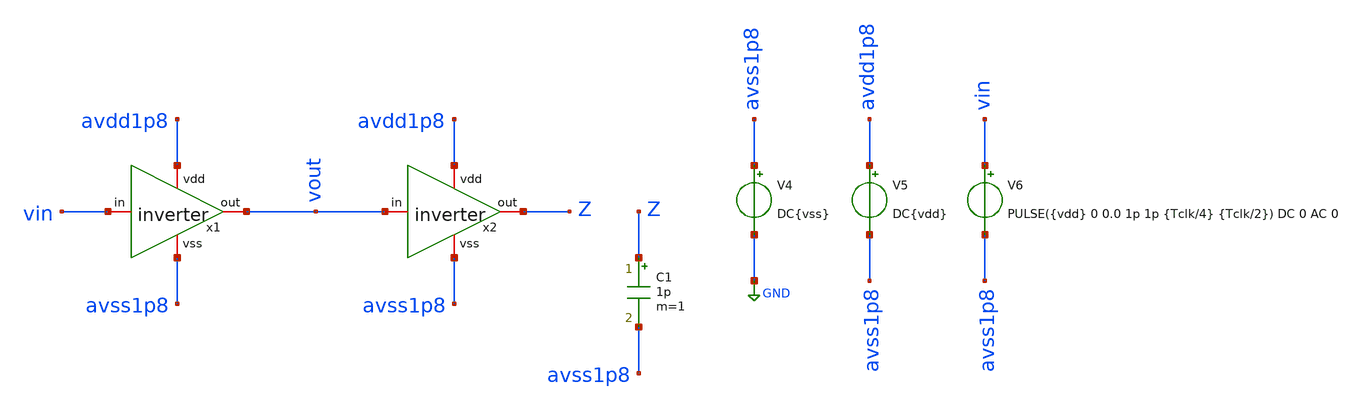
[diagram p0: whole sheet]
** sch_path: designs/sch/tests/tb_inverter.sch
**.subckt tb_inverter
V4 avss1p8 GND DC{vss}
V5 avdd1p8 avss1p8 DC{vdd}
V6 vin avss1p8 PULSE({vdd} 0 0.0 1p 1p {Tclk/4} {Tclk/2}) DC 0 AC 0
x1 avdd1p8 vout vin avss1p8 inverter
x2 avdd1p8 Z vout avss1p8 inverter
C1 Z avss1p8 1p m=1
**** begin user architecture code


* Circuit Parameters
.param vdd = 1.8
.param vss = 0.0
.param Tclk = 10n
.options TEMP = 65.0

* Include Models
.lib /foss/pdks/sky130A/libs.tech/ngspice/sky130.lib.spice TT

* OP Parameters & Singals to save
.save all

* Simulations
.control
  tran 0.001n 10n
  setplot tran1
  plot v(vin) v(vout)+2
reset
  dc V6 0 1.8 0.01
  setplot dc
  plot vin vout ylabel vout xlabel vin
  set filetype = ascii
  write dcsweep.raw
.endc

.end


**** end user architecture code
**.ends

* expanding   symbol:  /foss/designs/sch/inverter.sym # of pins=4
** sym_path: designs/inverter.sym
** sch_path: designs/inverter.sch
.subckt inverter vdd out in vss
*.iopin out
*.iopin vss
*.iopin vdd
*.iopin in
XM2 out in vss vss sky130_fd_pr__nfet_01v8 L=0.15 W=0.75 nf=1 ad='int((nf+1)/2) * W/nf * 0.29' as='int((nf+2)/2) * W/nf * 0.29'
+ pd='2*int((nf+1)/2) * (W/nf + 0.29)' ps='2*int((nf+2)/2) * (W/nf + 0.29)' nrd='0.29 / W' nrs='0.29 / W'
+ sa=0 sb=0 sd=0 mult=1 m=1
XM1 out in vdd vdd sky130_fd_pr__pfet_01v8 L=0.15 W=1.5 nf=1 ad='int((nf+1)/2) * W/nf * 0.29' as='int((nf+2)/2) * W/nf * 0.29'
+ pd='2*int((nf+1)/2) * (W/nf + 0.29)' ps='2*int((nf+2)/2) * (W/nf + 0.29)' nrd='0.29 / W' nrs='0.29 / W'
+ sa=0 sb=0 sd=0 mult=1 m=1
.ends

.GLOBAL GND
.end
